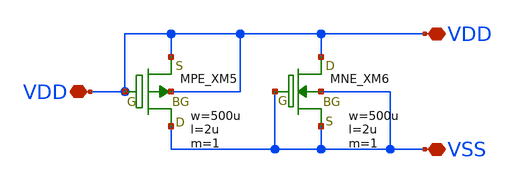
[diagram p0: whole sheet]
** sch_path: libs.tech/xschem/TR-1um_frame/OSS_ESD_5V_VDD.sch
**.subckt OSS_ESD_5V_VDD VSS VDD VDD
*.iopin VSS
*.iopin VDD
*.iopin VDD
XXM5 VSS VDD VDD VDD MPE w=500u l=2u as=0 ad=0 ps=0 pd=0 nrd=0 nrs=0 m=1
XXM6 VDD VSS VSS VSS MNE w=500u l=2u as=0 ad=0 ps=0 pd=0 nrd=0 nrs=0 m=1
**.ends
.end
